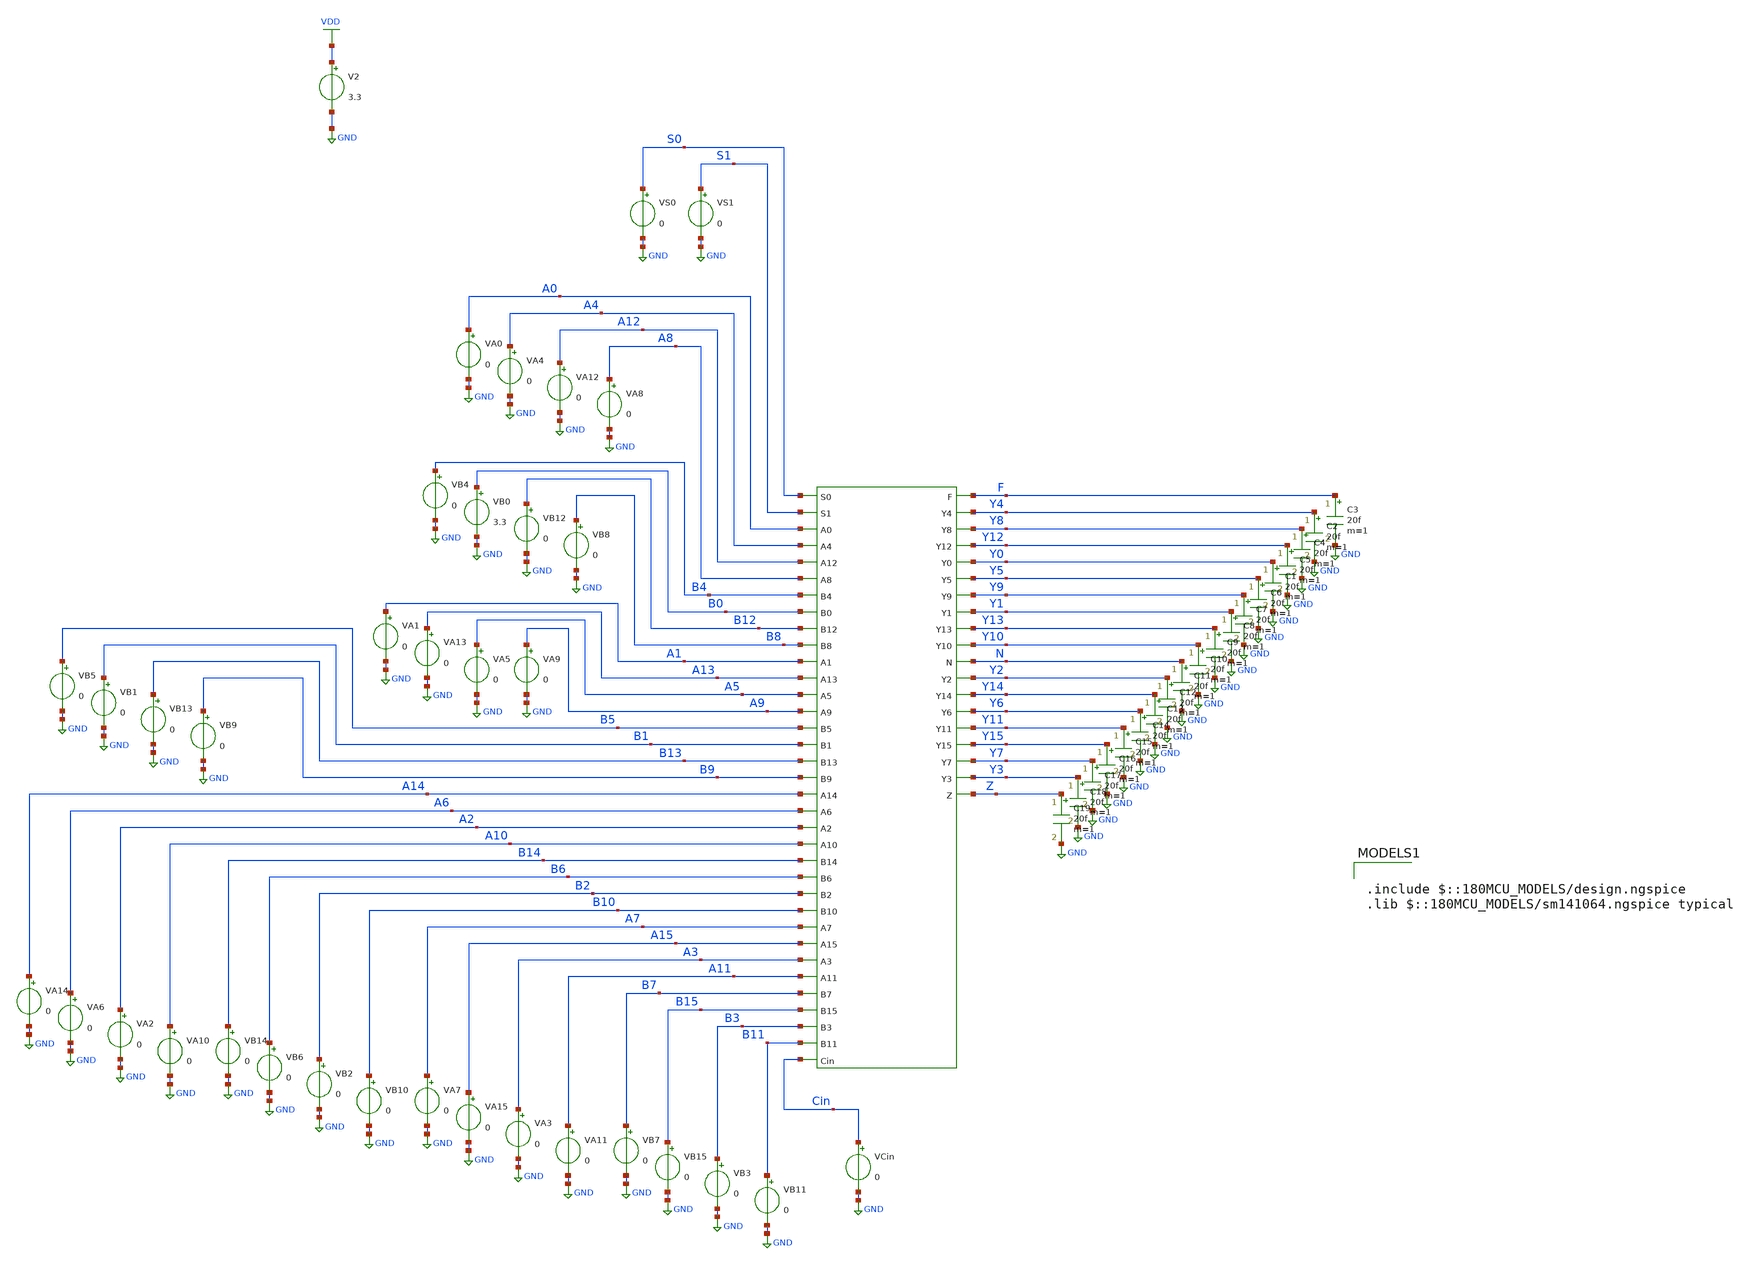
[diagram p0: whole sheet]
** sch_path: tbs/alu_tb.sch
**.subckt alu_tb
VA0 A0 GND 0
VA4 A4 GND 0
VA12 A12 GND 0
VA8 A8 GND 0
VA1 A1 GND 0
VA13 A13 GND 0
VA5 A5 GND 0
VA9 A9 GND 0
VA14 A14 GND 0
VA6 A6 GND 0
VA2 A2 GND 0
VA10 A10 GND 0
VA7 A7 GND 0
VA15 A15 GND 0
VA3 A3 GND 0
VA11 A11 GND 0
VB4 B4 GND 0
VB0 B0 GND 3.3
VB12 B12 GND 0
VB8 B8 GND 0
VB5 B5 GND 0
VB1 B1 GND 0
VB13 B13 GND 0
VB9 B9 GND 0
VB14 B14 GND 0
VB6 B6 GND 0
VB2 B2 GND 0
VB10 B10 GND 0
VB7 B7 GND 0
VB15 B15 GND 0
VB3 B3 GND 0
VB11 B11 GND 0
VCin Cin GND 0
VS1 S1 GND 0
VS0 S0 GND 0
C3 F GND 20f m=1
C2 Y4 GND 20f m=1
C4 Y8 GND 20f m=1
C5 Y12 GND 20f m=1
C1 Y0 GND 20f m=1
C6 Y5 GND 20f m=1
C7 Y9 GND 20f m=1
C8 Y1 GND 20f m=1
C9 Y13 GND 20f m=1
C10 Y10 GND 20f m=1
C11 N GND 20f m=1
C12 Y2 GND 20f m=1
C13 Y14 GND 20f m=1
C14 Y6 GND 20f m=1
C15 Y11 GND 20f m=1
C16 Y15 GND 20f m=1
C17 Y7 GND 20f m=1
C18 Y3 GND 20f m=1
C19 Z GND 20f m=1
V2 VDD GND 3.3
**** begin user architecture code


.control
  let vlow = 0
  let vhigh = 3.3

  * ADD mode
  alter VS1 = $&vlow
  alter VS0 = $&vlow

  * Carry in = 0
  alter VCin = $&vlow

  * A = 0x0003
  alter VA15 = $&vlow
  alter VA14 = $&vlow
  alter VA13 = $&vlow
  alter VA12 = $&vlow
  alter VA11 = $&vlow
  alter VA10 = $&vlow
  alter VA9  = $&vlow
  alter VA8  = $&vlow
  alter VA7  = $&vlow
  alter VA6  = $&vlow
  alter VA5  = $&vlow
  alter VA4  = $&vlow
  alter VA3  = $&vlow
  alter VA2  = $&vlow
  alter VA1  = $&vlow
  alter VA0  = $&vlow

  * B = 0x0005
  alter VB15 = $&vlow
  alter VB14 = $&vlow
  alter VB13 = $&vlow
  alter VB12 = $&vlow
  alter VB11 = $&vlow
  alter VB10 = $&vlow
  alter VB9  = $&vlow
  alter VB8  = $&vlow
  alter VB7  = $&vlow
  alter VB6  = $&vlow
  alter VB5  = $&vlow
  alter VB4  = $&vlow
  alter VB3  = $&vlow
  alter VB2  = $&vlow
  alter VB1  = $&vlow
  alter VB0  = $&vhigh

  * Solve DC operating point first
  * op

  * Print only the bits that matter for 3 + 5 = 8
  echo EXPECTED: Y3=3.3, Y2=0, Y1=0, Y0=0, F=0
  print v(y3) v(y2) v(y1) v(y0) v(f) v(z) v(n)
  * Optional very short transient, just for waveform screenshot
  tran 0.1n 10n
display
  plot v(y15) v(y14) v(y13) v(y12) v(y11) v(y10) v(y9) v(y8) v(y7) v(y6) v(y5) v(y4) v(y3) v(y2)
+ v(y1) v(y0)
  write alu_add_results.raw
.endc



.include $::180MCU_MODELS/design.ngspice
.lib $::180MCU_MODELS/sm141064.ngspice typical

**** end user architecture code
**.ends
.GLOBAL GND
.GLOBAL VDD
.end
